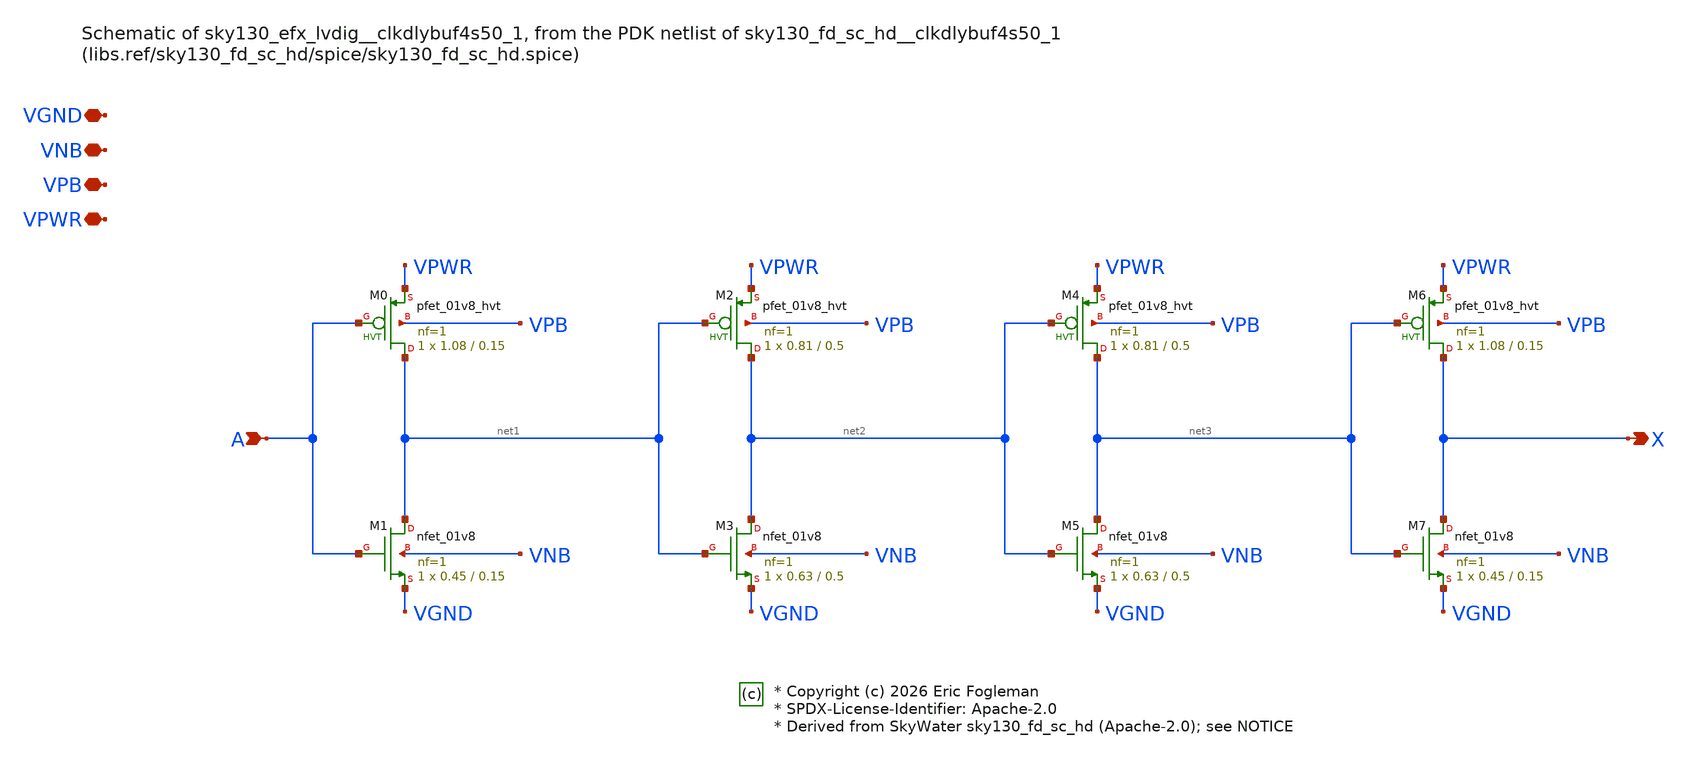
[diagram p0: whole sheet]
** sch_path: xschem/sky130_efx_lvdig__clkdlybuf4s50_1.sch

* Copyright (c) 2026 Eric Fogleman
* SPDX-License-Identifier: Apache-2.0
* Derived from SkyWater sky130_fd_sc_hd (Apache-2.0); see NOTICE

**.subckt sky130_efx_lvdig__clkdlybuf4s50_1 A X VGND VNB VPB VPWR
*.ipin A
*.opin X
*.iopin VGND
*.iopin VNB
*.iopin VPB
*.iopin VPWR
XM0 net1 A VPWR VPB sky130_fd_pr__pfet_01v8_hvt L=0.15 W=1.08 nf=1 ad='int((1 + 1)/2) * 1.08 / 1 * 0.29'
+ as='int((1 + 2)/2) * 1.08 / 1 * 0.29' pd='2*int((1 + 1)/2) * (1.08 / 1 + 0.29)' ps='2*int((1 + 2)/2) * (1.08 / 1 + 0.29)'
+ nrd='0.29 / 1.08 ' nrs='0.29 / 1.08 ' sa=0 sb=0 sd=0 mult=1 m=1
XM1 net1 A VGND VNB sky130_fd_pr__nfet_01v8 L=0.15 W=0.45 nf=1 ad='int((1 + 1)/2) * 0.45 / 1 * 0.29'
+ as='int((1 + 2)/2) * 0.45 / 1 * 0.29' pd='2*int((1 + 1)/2) * (0.45 / 1 + 0.29)' ps='2*int((1 + 2)/2) * (0.45 / 1 + 0.29)'
+ nrd='0.29 / 0.45 ' nrs='0.29 / 0.45 ' sa=0 sb=0 sd=0 mult=1 m=1
XM2 net2 net1 VPWR VPB sky130_fd_pr__pfet_01v8_hvt L=0.5 W=0.81 nf=1 ad='int((1 + 1)/2) * 0.81 / 1 * 0.29'
+ as='int((1 + 2)/2) * 0.81 / 1 * 0.29' pd='2*int((1 + 1)/2) * (0.81 / 1 + 0.29)' ps='2*int((1 + 2)/2) * (0.81 / 1 + 0.29)'
+ nrd='0.29 / 0.81 ' nrs='0.29 / 0.81 ' sa=0 sb=0 sd=0 mult=1 m=1
XM3 net2 net1 VGND VNB sky130_fd_pr__nfet_01v8 L=0.5 W=0.63 nf=1 ad='int((1 + 1)/2) * 0.63 / 1 * 0.29'
+ as='int((1 + 2)/2) * 0.63 / 1 * 0.29' pd='2*int((1 + 1)/2) * (0.63 / 1 + 0.29)' ps='2*int((1 + 2)/2) * (0.63 / 1 + 0.29)'
+ nrd='0.29 / 0.63 ' nrs='0.29 / 0.63 ' sa=0 sb=0 sd=0 mult=1 m=1
XM4 net3 net2 VPWR VPB sky130_fd_pr__pfet_01v8_hvt L=0.5 W=0.81 nf=1 ad='int((1 + 1)/2) * 0.81 / 1 * 0.29'
+ as='int((1 + 2)/2) * 0.81 / 1 * 0.29' pd='2*int((1 + 1)/2) * (0.81 / 1 + 0.29)' ps='2*int((1 + 2)/2) * (0.81 / 1 + 0.29)'
+ nrd='0.29 / 0.81 ' nrs='0.29 / 0.81 ' sa=0 sb=0 sd=0 mult=1 m=1
XM5 net3 net2 VGND VNB sky130_fd_pr__nfet_01v8 L=0.5 W=0.63 nf=1 ad='int((1 + 1)/2) * 0.63 / 1 * 0.29'
+ as='int((1 + 2)/2) * 0.63 / 1 * 0.29' pd='2*int((1 + 1)/2) * (0.63 / 1 + 0.29)' ps='2*int((1 + 2)/2) * (0.63 / 1 + 0.29)'
+ nrd='0.29 / 0.63 ' nrs='0.29 / 0.63 ' sa=0 sb=0 sd=0 mult=1 m=1
XM6 X net3 VPWR VPB sky130_fd_pr__pfet_01v8_hvt L=0.15 W=1.08 nf=1 ad='int((1 + 1)/2) * 1.08 / 1 * 0.29'
+ as='int((1 + 2)/2) * 1.08 / 1 * 0.29' pd='2*int((1 + 1)/2) * (1.08 / 1 + 0.29)' ps='2*int((1 + 2)/2) * (1.08 / 1 + 0.29)'
+ nrd='0.29 / 1.08 ' nrs='0.29 / 1.08 ' sa=0 sb=0 sd=0 mult=1 m=1
XM7 X net3 VGND VNB sky130_fd_pr__nfet_01v8 L=0.15 W=0.45 nf=1 ad='int((1 + 1)/2) * 0.45 / 1 * 0.29'
+ as='int((1 + 2)/2) * 0.45 / 1 * 0.29' pd='2*int((1 + 1)/2) * (0.45 / 1 + 0.29)' ps='2*int((1 + 2)/2) * (0.45 / 1 + 0.29)'
+ nrd='0.29 / 0.45 ' nrs='0.29 / 0.45 ' sa=0 sb=0 sd=0 mult=1 m=1
**.ends
.end
